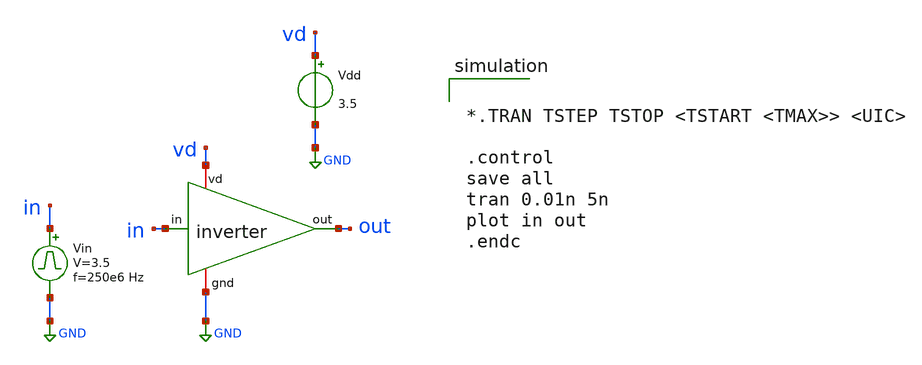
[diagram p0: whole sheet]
** sch_path: xschem_files/inverter_tb_tran.sch
**.subckt inverter_tb_tran
x1 vd in out GND inverter
Vin in GND pulse 0 3.5 '0.495/ 250e6 ' '0.01/250e6 ' '0.01/250e6 ' '0.49/250e6 ' '1/250e6 '
Vdd vd GND 3.5
**** begin user architecture code


*.TRAN TSTEP TSTOP <TSTART <TMAX>> <UIC>

.control
save all
tran 0.01n 5n
plot in out
.endc



** opencircuitdesign pdks install
.lib $::SKYWATER_MODELS/sky130.lib.spice tt


**** end user architecture code
**.ends

* expanding   symbol:  /home/hadassaju/prjects/inverter.sym # of pins=4
** sym_path: xschem_files/inverter.sym
** sch_path: xschem_files/inverter.sch
.subckt inverter vd in out gnd
*.ipin in
*.opin out
*.iopin vd
*.iopin gnd
XN0 out in gnd gnd sky130_fd_pr__nfet_01v8 L=0.15 W=1 nf=1 ad='int((nf+1)/2) * W/nf * 0.29' as='int((nf+2)/2) * W/nf * 0.29'
+ pd='2*int((nf+1)/2) * (W/nf + 0.29)' ps='2*int((nf+2)/2) * (W/nf + 0.29)' nrd='0.29 / W' nrs='0.29 / W'
+ sa=0 sb=0 sd=0 mult=1 m=1
XP0 out in vd vd sky130_fd_pr__pfet_01v8 L=0.15 W=3 nf=1 ad='int((nf+1)/2) * W/nf * 0.29' as='int((nf+2)/2) * W/nf * 0.29'
+ pd='2*int((nf+1)/2) * (W/nf + 0.29)' ps='2*int((nf+2)/2) * (W/nf + 0.29)' nrd='0.29 / W' nrs='0.29 / W'
+ sa=0 sb=0 sd=0 mult=1 m=1
.ends

.GLOBAL GND
.end
